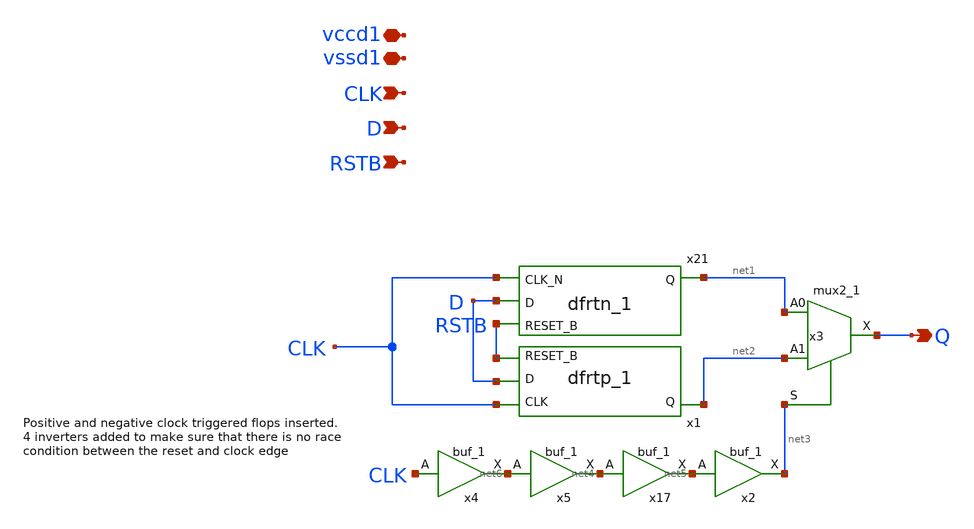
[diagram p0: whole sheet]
** sch_path: xschem/digital/deff_rst_vccd.sch
**.subckt deff_rst_vccd CLK D Q RSTB vccd1 vssd1
*.ipin CLK
*.ipin D
*.opin Q
*.ipin RSTB
*.iopin vccd1
*.iopin vssd1
x3 net1 net2 net3 vssd1 vssd1 vccd1 vccd1 Q sky130_fd_sc_hd__mux2_1
x21 CLK D RSTB vssd1 vssd1 vccd1 vccd1 net1 sky130_fd_sc_hd__dfrtn_1
x1 CLK D RSTB vssd1 vssd1 vccd1 vccd1 net2 sky130_fd_sc_hd__dfrtp_1
x17 net4 vssd1 vssd1 vccd1 vccd1 net5 sky130_fd_sc_hd__buf_1
x2 net5 vssd1 vssd1 vccd1 vccd1 net3 sky130_fd_sc_hd__buf_1
x4 CLK vssd1 vssd1 vccd1 vccd1 net6 sky130_fd_sc_hd__buf_1
x5 net6 vssd1 vssd1 vccd1 vccd1 net4 sky130_fd_sc_hd__buf_1
**.ends
.end
